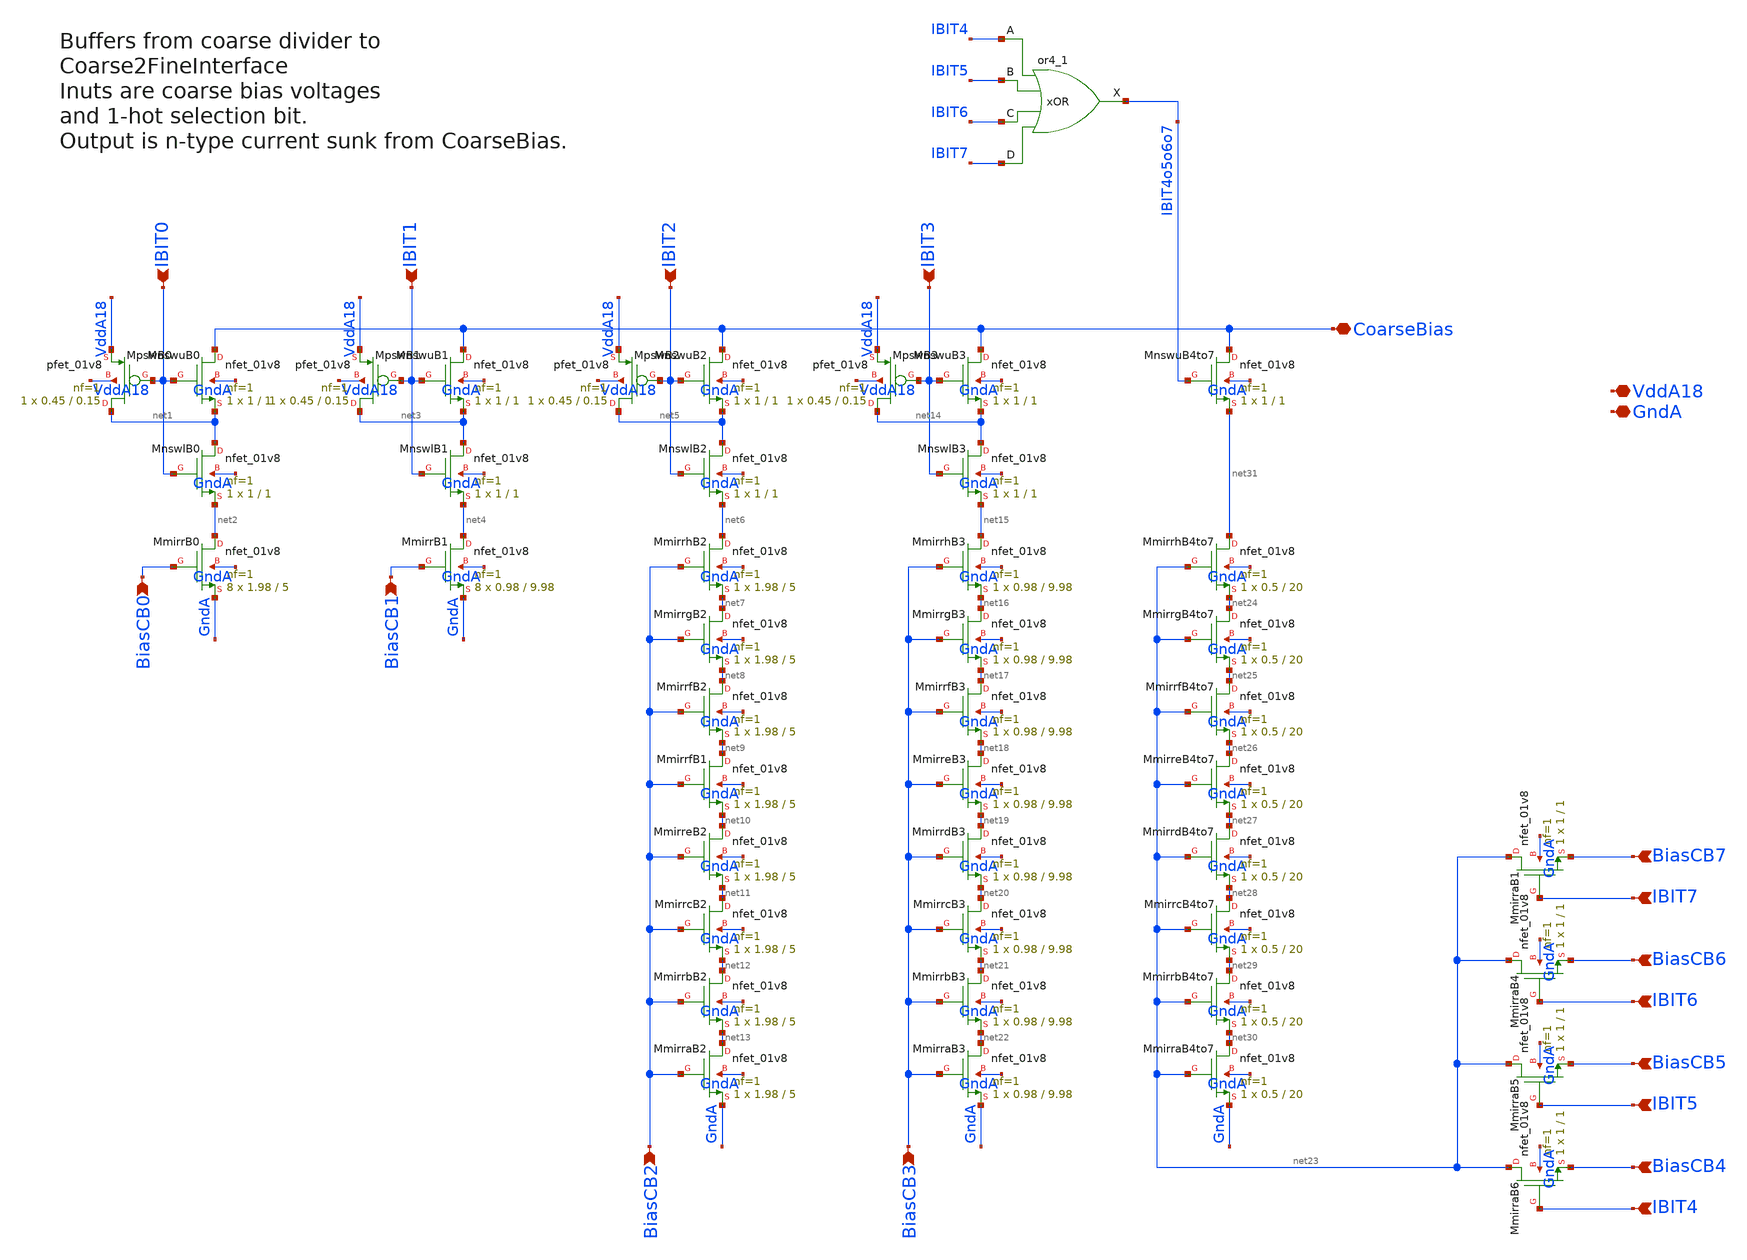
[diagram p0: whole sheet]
** sch_path: analog/xschem/BiasCoarseSel8to1.sch
**.subckt BiasCoarseSel8to1 IBIT0 BiasCB0 IBIT1 BiasCB1 IBIT2 BiasCB2 IBIT3 BiasCB3 BiasCB7 IBIT7
*+ BiasCB6 IBIT6 BiasCB5 IBIT5 BiasCB4 IBIT4 CoarseBias VddA18 GndA
*.ipin IBIT0
*.ipin BiasCB0
*.ipin IBIT1
*.ipin BiasCB1
*.ipin IBIT2
*.ipin BiasCB2
*.ipin IBIT3
*.ipin BiasCB3
*.ipin BiasCB7
*.ipin IBIT7
*.ipin BiasCB6
*.ipin IBIT6
*.ipin BiasCB5
*.ipin IBIT5
*.ipin BiasCB4
*.ipin IBIT4
*.iopin CoarseBias
*.iopin VddA18
*.iopin GndA
xOR IBIT4 IBIT5 IBIT6 IBIT7 GndA GndA VddA18 VddA18 IBIT4o5o6o7 sky130_fd_sc_hd__or4_1
XMpswB0 net1 IBIT0 VddA18 VddA18 sky130_fd_pr__pfet_01v8 L=0.15 W=0.45 nf=1 ad='int((1 + 1)/2) * 0.45 / 1 * 0.29'
+ as='int((1 + 2)/2) * 0.45 / 1 * 0.29' pd='2*int((1 + 1)/2) * (0.45 / 1 + 0.29)' ps='2*int((1 + 2)/2) * (0.45 / 1 + 0.29)'
+ nrd='0.29 / 0.45 ' nrs='0.29 / 0.45 ' sa=0 sb=0 sd=0 mult=1 m=1
XMnswuB0 CoarseBias IBIT0 net1 GndA sky130_fd_pr__nfet_01v8 L=1 W=1 nf=1 ad='int((1 + 1)/2) * 1 / 1 * 0.29'
+ as='int((1 + 2)/2) * 1 / 1 * 0.29' pd='2*int((1 + 1)/2) * (1 / 1 + 0.29)' ps='2*int((1 + 2)/2) * (1 / 1 + 0.29)'
+ nrd='0.29 / 1 ' nrs='0.29 / 1 ' sa=0 sb=0 sd=0 mult=1 m=1
XMnswlB0 net1 IBIT0 net2 GndA sky130_fd_pr__nfet_01v8 L=1 W=1 nf=1 ad='int((1 + 1)/2) * 1 / 1 * 0.29'
+ as='int((1 + 2)/2) * 1 / 1 * 0.29' pd='2*int((1 + 1)/2) * (1 / 1 + 0.29)' ps='2*int((1 + 2)/2) * (1 / 1 + 0.29)'
+ nrd='0.29 / 1 ' nrs='0.29 / 1 ' sa=0 sb=0 sd=0 mult=1 m=1
XMmirrB0 net2 BiasCB0 GndA GndA sky130_fd_pr__nfet_01v8 L=5 W=1.98 nf=1 ad='int((1 + 1)/2) * 1.98 / 1 * 0.29'
+ as='int((1 + 2)/2) * 1.98 / 1 * 0.29' pd='2*int((1 + 1)/2) * (1.98 / 1 + 0.29)' ps='2*int((1 + 2)/2) * (1.98 / 1 + 0.29)'
+ nrd='0.29 / 1.98 ' nrs='0.29 / 1.98 ' sa=0 sb=0 sd=0 mult=8 m=8
XMpswB1 net3 IBIT1 VddA18 VddA18 sky130_fd_pr__pfet_01v8 L=0.15 W=0.45 nf=1 ad='int((1 + 1)/2) * 0.45 / 1 * 0.29'
+ as='int((1 + 2)/2) * 0.45 / 1 * 0.29' pd='2*int((1 + 1)/2) * (0.45 / 1 + 0.29)' ps='2*int((1 + 2)/2) * (0.45 / 1 + 0.29)'
+ nrd='0.29 / 0.45 ' nrs='0.29 / 0.45 ' sa=0 sb=0 sd=0 mult=1 m=1
XMnswuB1 CoarseBias IBIT1 net3 GndA sky130_fd_pr__nfet_01v8 L=1 W=1 nf=1 ad='int((1 + 1)/2) * 1 / 1 * 0.29'
+ as='int((1 + 2)/2) * 1 / 1 * 0.29' pd='2*int((1 + 1)/2) * (1 / 1 + 0.29)' ps='2*int((1 + 2)/2) * (1 / 1 + 0.29)'
+ nrd='0.29 / 1 ' nrs='0.29 / 1 ' sa=0 sb=0 sd=0 mult=1 m=1
XMnswlB1 net3 IBIT1 net4 GndA sky130_fd_pr__nfet_01v8 L=1 W=1 nf=1 ad='int((1 + 1)/2) * 1 / 1 * 0.29'
+ as='int((1 + 2)/2) * 1 / 1 * 0.29' pd='2*int((1 + 1)/2) * (1 / 1 + 0.29)' ps='2*int((1 + 2)/2) * (1 / 1 + 0.29)'
+ nrd='0.29 / 1 ' nrs='0.29 / 1 ' sa=0 sb=0 sd=0 mult=1 m=1
XMmirrB1 net4 BiasCB1 GndA GndA sky130_fd_pr__nfet_01v8 L=9.98 W=0.98 nf=1 ad='int((1 + 1)/2) * 0.98 / 1 * 0.29'
+ as='int((1 + 2)/2) * 0.98 / 1 * 0.29' pd='2*int((1 + 1)/2) * (0.98 / 1 + 0.29)' ps='2*int((1 + 2)/2) * (0.98 / 1 + 0.29)'
+ nrd='0.29 / 0.98 ' nrs='0.29 / 0.98 ' sa=0 sb=0 sd=0 mult=8 m=8
XMpswB2 net5 IBIT2 VddA18 VddA18 sky130_fd_pr__pfet_01v8 L=0.15 W=0.45 nf=1 ad='int((1 + 1)/2) * 0.45 / 1 * 0.29'
+ as='int((1 + 2)/2) * 0.45 / 1 * 0.29' pd='2*int((1 + 1)/2) * (0.45 / 1 + 0.29)' ps='2*int((1 + 2)/2) * (0.45 / 1 + 0.29)'
+ nrd='0.29 / 0.45 ' nrs='0.29 / 0.45 ' sa=0 sb=0 sd=0 mult=1 m=1
XMnswuB2 CoarseBias IBIT2 net5 GndA sky130_fd_pr__nfet_01v8 L=1 W=1 nf=1 ad='int((1 + 1)/2) * 1 / 1 * 0.29'
+ as='int((1 + 2)/2) * 1 / 1 * 0.29' pd='2*int((1 + 1)/2) * (1 / 1 + 0.29)' ps='2*int((1 + 2)/2) * (1 / 1 + 0.29)'
+ nrd='0.29 / 1 ' nrs='0.29 / 1 ' sa=0 sb=0 sd=0 mult=1 m=1
XMnswlB2 net5 IBIT2 net6 GndA sky130_fd_pr__nfet_01v8 L=1 W=1 nf=1 ad='int((1 + 1)/2) * 1 / 1 * 0.29'
+ as='int((1 + 2)/2) * 1 / 1 * 0.29' pd='2*int((1 + 1)/2) * (1 / 1 + 0.29)' ps='2*int((1 + 2)/2) * (1 / 1 + 0.29)'
+ nrd='0.29 / 1 ' nrs='0.29 / 1 ' sa=0 sb=0 sd=0 mult=1 m=1
XMmirrhB2 net6 BiasCB2 net7 GndA sky130_fd_pr__nfet_01v8 L=5 W=1.98 nf=1 ad='int((1 + 1)/2) * 1.98 / 1 * 0.29'
+ as='int((1 + 2)/2) * 1.98 / 1 * 0.29' pd='2*int((1 + 1)/2) * (1.98 / 1 + 0.29)' ps='2*int((1 + 2)/2) * (1.98 / 1 + 0.29)'
+ nrd='0.29 / 1.98 ' nrs='0.29 / 1.98 ' sa=0 sb=0 sd=0 mult=1 m=1
XMmirrgB2 net7 BiasCB2 net8 GndA sky130_fd_pr__nfet_01v8 L=5 W=1.98 nf=1 ad='int((1 + 1)/2) * 1.98 / 1 * 0.29'
+ as='int((1 + 2)/2) * 1.98 / 1 * 0.29' pd='2*int((1 + 1)/2) * (1.98 / 1 + 0.29)' ps='2*int((1 + 2)/2) * (1.98 / 1 + 0.29)'
+ nrd='0.29 / 1.98 ' nrs='0.29 / 1.98 ' sa=0 sb=0 sd=0 mult=1 m=1
XMmirrfB2 net8 BiasCB2 net9 GndA sky130_fd_pr__nfet_01v8 L=5 W=1.98 nf=1 ad='int((1 + 1)/2) * 1.98 / 1 * 0.29'
+ as='int((1 + 2)/2) * 1.98 / 1 * 0.29' pd='2*int((1 + 1)/2) * (1.98 / 1 + 0.29)' ps='2*int((1 + 2)/2) * (1.98 / 1 + 0.29)'
+ nrd='0.29 / 1.98 ' nrs='0.29 / 1.98 ' sa=0 sb=0 sd=0 mult=1 m=1
XMmirrfB1 net9 BiasCB2 net10 GndA sky130_fd_pr__nfet_01v8 L=5 W=1.98 nf=1 ad='int((1 + 1)/2) * 1.98 / 1 * 0.29'
+ as='int((1 + 2)/2) * 1.98 / 1 * 0.29' pd='2*int((1 + 1)/2) * (1.98 / 1 + 0.29)' ps='2*int((1 + 2)/2) * (1.98 / 1 + 0.29)'
+ nrd='0.29 / 1.98 ' nrs='0.29 / 1.98 ' sa=0 sb=0 sd=0 mult=1 m=1
XMmirreB2 net10 BiasCB2 net11 GndA sky130_fd_pr__nfet_01v8 L=5 W=1.98 nf=1 ad='int((1 + 1)/2) * 1.98 / 1 * 0.29'
+ as='int((1 + 2)/2) * 1.98 / 1 * 0.29' pd='2*int((1 + 1)/2) * (1.98 / 1 + 0.29)' ps='2*int((1 + 2)/2) * (1.98 / 1 + 0.29)'
+ nrd='0.29 / 1.98 ' nrs='0.29 / 1.98 ' sa=0 sb=0 sd=0 mult=1 m=1
XMmirrcB2 net11 BiasCB2 net12 GndA sky130_fd_pr__nfet_01v8 L=5 W=1.98 nf=1 ad='int((1 + 1)/2) * 1.98 / 1 * 0.29'
+ as='int((1 + 2)/2) * 1.98 / 1 * 0.29' pd='2*int((1 + 1)/2) * (1.98 / 1 + 0.29)' ps='2*int((1 + 2)/2) * (1.98 / 1 + 0.29)'
+ nrd='0.29 / 1.98 ' nrs='0.29 / 1.98 ' sa=0 sb=0 sd=0 mult=1 m=1
XMmirrbB2 net12 BiasCB2 net13 GndA sky130_fd_pr__nfet_01v8 L=5 W=1.98 nf=1 ad='int((1 + 1)/2) * 1.98 / 1 * 0.29'
+ as='int((1 + 2)/2) * 1.98 / 1 * 0.29' pd='2*int((1 + 1)/2) * (1.98 / 1 + 0.29)' ps='2*int((1 + 2)/2) * (1.98 / 1 + 0.29)'
+ nrd='0.29 / 1.98 ' nrs='0.29 / 1.98 ' sa=0 sb=0 sd=0 mult=1 m=1
XMmirraB2 net13 BiasCB2 GndA GndA sky130_fd_pr__nfet_01v8 L=5 W=1.98 nf=1 ad='int((1 + 1)/2) * 1.98 / 1 * 0.29'
+ as='int((1 + 2)/2) * 1.98 / 1 * 0.29' pd='2*int((1 + 1)/2) * (1.98 / 1 + 0.29)' ps='2*int((1 + 2)/2) * (1.98 / 1 + 0.29)'
+ nrd='0.29 / 1.98 ' nrs='0.29 / 1.98 ' sa=0 sb=0 sd=0 mult=1 m=1
XMpswB3 net14 IBIT3 VddA18 VddA18 sky130_fd_pr__pfet_01v8 L=0.15 W=0.45 nf=1 ad='int((1 + 1)/2) * 0.45 / 1 * 0.29'
+ as='int((1 + 2)/2) * 0.45 / 1 * 0.29' pd='2*int((1 + 1)/2) * (0.45 / 1 + 0.29)' ps='2*int((1 + 2)/2) * (0.45 / 1 + 0.29)'
+ nrd='0.29 / 0.45 ' nrs='0.29 / 0.45 ' sa=0 sb=0 sd=0 mult=1 m=1
XMnswuB3 CoarseBias IBIT3 net14 GndA sky130_fd_pr__nfet_01v8 L=1 W=1 nf=1 ad='int((1 + 1)/2) * 1 / 1 * 0.29'
+ as='int((1 + 2)/2) * 1 / 1 * 0.29' pd='2*int((1 + 1)/2) * (1 / 1 + 0.29)' ps='2*int((1 + 2)/2) * (1 / 1 + 0.29)'
+ nrd='0.29 / 1 ' nrs='0.29 / 1 ' sa=0 sb=0 sd=0 mult=1 m=1
XMnswlB3 net14 IBIT3 net15 GndA sky130_fd_pr__nfet_01v8 L=1 W=1 nf=1 ad='int((1 + 1)/2) * 1 / 1 * 0.29'
+ as='int((1 + 2)/2) * 1 / 1 * 0.29' pd='2*int((1 + 1)/2) * (1 / 1 + 0.29)' ps='2*int((1 + 2)/2) * (1 / 1 + 0.29)'
+ nrd='0.29 / 1 ' nrs='0.29 / 1 ' sa=0 sb=0 sd=0 mult=1 m=1
XMmirrhB3 net15 BiasCB3 net16 GndA sky130_fd_pr__nfet_01v8 L=9.98 W=0.98 nf=1 ad='int((1 + 1)/2) * 0.98 / 1 * 0.29'
+ as='int((1 + 2)/2) * 0.98 / 1 * 0.29' pd='2*int((1 + 1)/2) * (0.98 / 1 + 0.29)' ps='2*int((1 + 2)/2) * (0.98 / 1 + 0.29)'
+ nrd='0.29 / 0.98 ' nrs='0.29 / 0.98 ' sa=0 sb=0 sd=0 mult=1 m=1
XMmirrgB3 net16 BiasCB3 net17 GndA sky130_fd_pr__nfet_01v8 L=9.98 W=0.98 nf=1 ad='int((1 + 1)/2) * 0.98 / 1 * 0.29'
+ as='int((1 + 2)/2) * 0.98 / 1 * 0.29' pd='2*int((1 + 1)/2) * (0.98 / 1 + 0.29)' ps='2*int((1 + 2)/2) * (0.98 / 1 + 0.29)'
+ nrd='0.29 / 0.98 ' nrs='0.29 / 0.98 ' sa=0 sb=0 sd=0 mult=1 m=1
XMmirrfB3 net17 BiasCB3 net18 GndA sky130_fd_pr__nfet_01v8 L=9.98 W=0.98 nf=1 ad='int((1 + 1)/2) * 0.98 / 1 * 0.29'
+ as='int((1 + 2)/2) * 0.98 / 1 * 0.29' pd='2*int((1 + 1)/2) * (0.98 / 1 + 0.29)' ps='2*int((1 + 2)/2) * (0.98 / 1 + 0.29)'
+ nrd='0.29 / 0.98 ' nrs='0.29 / 0.98 ' sa=0 sb=0 sd=0 mult=1 m=1
XMmirreB3 net18 BiasCB3 net19 GndA sky130_fd_pr__nfet_01v8 L=9.98 W=0.98 nf=1 ad='int((1 + 1)/2) * 0.98 / 1 * 0.29'
+ as='int((1 + 2)/2) * 0.98 / 1 * 0.29' pd='2*int((1 + 1)/2) * (0.98 / 1 + 0.29)' ps='2*int((1 + 2)/2) * (0.98 / 1 + 0.29)'
+ nrd='0.29 / 0.98 ' nrs='0.29 / 0.98 ' sa=0 sb=0 sd=0 mult=1 m=1
XMmirrdB3 net19 BiasCB3 net20 GndA sky130_fd_pr__nfet_01v8 L=9.98 W=0.98 nf=1 ad='int((1 + 1)/2) * 0.98 / 1 * 0.29'
+ as='int((1 + 2)/2) * 0.98 / 1 * 0.29' pd='2*int((1 + 1)/2) * (0.98 / 1 + 0.29)' ps='2*int((1 + 2)/2) * (0.98 / 1 + 0.29)'
+ nrd='0.29 / 0.98 ' nrs='0.29 / 0.98 ' sa=0 sb=0 sd=0 mult=1 m=1
XMmirrcB3 net20 BiasCB3 net21 GndA sky130_fd_pr__nfet_01v8 L=9.98 W=0.98 nf=1 ad='int((1 + 1)/2) * 0.98 / 1 * 0.29'
+ as='int((1 + 2)/2) * 0.98 / 1 * 0.29' pd='2*int((1 + 1)/2) * (0.98 / 1 + 0.29)' ps='2*int((1 + 2)/2) * (0.98 / 1 + 0.29)'
+ nrd='0.29 / 0.98 ' nrs='0.29 / 0.98 ' sa=0 sb=0 sd=0 mult=1 m=1
XMmirrbB3 net21 BiasCB3 net22 GndA sky130_fd_pr__nfet_01v8 L=9.98 W=0.98 nf=1 ad='int((1 + 1)/2) * 0.98 / 1 * 0.29'
+ as='int((1 + 2)/2) * 0.98 / 1 * 0.29' pd='2*int((1 + 1)/2) * (0.98 / 1 + 0.29)' ps='2*int((1 + 2)/2) * (0.98 / 1 + 0.29)'
+ nrd='0.29 / 0.98 ' nrs='0.29 / 0.98 ' sa=0 sb=0 sd=0 mult=1 m=1
XMmirraB3 net22 BiasCB3 GndA GndA sky130_fd_pr__nfet_01v8 L=9.98 W=0.98 nf=1 ad='int((1 + 1)/2) * 0.98 / 1 * 0.29'
+ as='int((1 + 2)/2) * 0.98 / 1 * 0.29' pd='2*int((1 + 1)/2) * (0.98 / 1 + 0.29)' ps='2*int((1 + 2)/2) * (0.98 / 1 + 0.29)'
+ nrd='0.29 / 0.98 ' nrs='0.29 / 0.98 ' sa=0 sb=0 sd=0 mult=1 m=1
XMnswuB4to7 CoarseBias IBIT4o5o6o7 net31 GndA sky130_fd_pr__nfet_01v8 L=1 W=1 nf=1 ad='int((1 + 1)/2) * 1 / 1 * 0.29'
+ as='int((1 + 2)/2) * 1 / 1 * 0.29' pd='2*int((1 + 1)/2) * (1 / 1 + 0.29)' ps='2*int((1 + 2)/2) * (1 / 1 + 0.29)'
+ nrd='0.29 / 1 ' nrs='0.29 / 1 ' sa=0 sb=0 sd=0 mult=1 m=1
XMmirrhB4to7 net31 net23 net24 GndA sky130_fd_pr__nfet_01v8 L=20 W=0.5 nf=1 ad='int((1 + 1)/2) * 0.5 / 1 * 0.29'
+ as='int((1 + 2)/2) * 0.5 / 1 * 0.29' pd='2*int((1 + 1)/2) * (0.5 / 1 + 0.29)' ps='2*int((1 + 2)/2) * (0.5 / 1 + 0.29)'
+ nrd='0.29 / 0.5 ' nrs='0.29 / 0.5 ' sa=0 sb=0 sd=0 mult=1 m=1
XMmirraB4to7 net30 net23 GndA GndA sky130_fd_pr__nfet_01v8 L=20 W=0.5 nf=1 ad='int((1 + 1)/2) * 0.5 / 1 * 0.29'
+ as='int((1 + 2)/2) * 0.5 / 1 * 0.29' pd='2*int((1 + 1)/2) * (0.5 / 1 + 0.29)' ps='2*int((1 + 2)/2) * (0.5 / 1 + 0.29)'
+ nrd='0.29 / 0.5 ' nrs='0.29 / 0.5 ' sa=0 sb=0 sd=0 mult=1 m=1
XMmirrbB4to7 net29 net23 net30 GndA sky130_fd_pr__nfet_01v8 L=20 W=0.5 nf=1 ad='int((1 + 1)/2) * 0.5 / 1 * 0.29'
+ as='int((1 + 2)/2) * 0.5 / 1 * 0.29' pd='2*int((1 + 1)/2) * (0.5 / 1 + 0.29)' ps='2*int((1 + 2)/2) * (0.5 / 1 + 0.29)'
+ nrd='0.29 / 0.5 ' nrs='0.29 / 0.5 ' sa=0 sb=0 sd=0 mult=1 m=1
XMmirrcB4to7 net28 net23 net29 GndA sky130_fd_pr__nfet_01v8 L=20 W=0.5 nf=1 ad='int((1 + 1)/2) * 0.5 / 1 * 0.29'
+ as='int((1 + 2)/2) * 0.5 / 1 * 0.29' pd='2*int((1 + 1)/2) * (0.5 / 1 + 0.29)' ps='2*int((1 + 2)/2) * (0.5 / 1 + 0.29)'
+ nrd='0.29 / 0.5 ' nrs='0.29 / 0.5 ' sa=0 sb=0 sd=0 mult=1 m=1
XMmirrdB4to7 net27 net23 net28 GndA sky130_fd_pr__nfet_01v8 L=20 W=0.5 nf=1 ad='int((1 + 1)/2) * 0.5 / 1 * 0.29'
+ as='int((1 + 2)/2) * 0.5 / 1 * 0.29' pd='2*int((1 + 1)/2) * (0.5 / 1 + 0.29)' ps='2*int((1 + 2)/2) * (0.5 / 1 + 0.29)'
+ nrd='0.29 / 0.5 ' nrs='0.29 / 0.5 ' sa=0 sb=0 sd=0 mult=1 m=1
XMmirreB4to7 net26 net23 net27 GndA sky130_fd_pr__nfet_01v8 L=20 W=0.5 nf=1 ad='int((1 + 1)/2) * 0.5 / 1 * 0.29'
+ as='int((1 + 2)/2) * 0.5 / 1 * 0.29' pd='2*int((1 + 1)/2) * (0.5 / 1 + 0.29)' ps='2*int((1 + 2)/2) * (0.5 / 1 + 0.29)'
+ nrd='0.29 / 0.5 ' nrs='0.29 / 0.5 ' sa=0 sb=0 sd=0 mult=1 m=1
XMmirrfB4to7 net25 net23 net26 GndA sky130_fd_pr__nfet_01v8 L=20 W=0.5 nf=1 ad='int((1 + 1)/2) * 0.5 / 1 * 0.29'
+ as='int((1 + 2)/2) * 0.5 / 1 * 0.29' pd='2*int((1 + 1)/2) * (0.5 / 1 + 0.29)' ps='2*int((1 + 2)/2) * (0.5 / 1 + 0.29)'
+ nrd='0.29 / 0.5 ' nrs='0.29 / 0.5 ' sa=0 sb=0 sd=0 mult=1 m=1
XMmirrgB4to7 net24 net23 net25 GndA sky130_fd_pr__nfet_01v8 L=20 W=0.5 nf=1 ad='int((1 + 1)/2) * 0.5 / 1 * 0.29'
+ as='int((1 + 2)/2) * 0.5 / 1 * 0.29' pd='2*int((1 + 1)/2) * (0.5 / 1 + 0.29)' ps='2*int((1 + 2)/2) * (0.5 / 1 + 0.29)'
+ nrd='0.29 / 0.5 ' nrs='0.29 / 0.5 ' sa=0 sb=0 sd=0 mult=1 m=1
XMmirraB1 net23 IBIT7 BiasCB7 GndA sky130_fd_pr__nfet_01v8 L=1 W=1 nf=1 ad='int((1 + 1)/2) * 1 / 1 * 0.29'
+ as='int((1 + 2)/2) * 1 / 1 * 0.29' pd='2*int((1 + 1)/2) * (1 / 1 + 0.29)' ps='2*int((1 + 2)/2) * (1 / 1 + 0.29)'
+ nrd='0.29 / 1 ' nrs='0.29 / 1 ' sa=0 sb=0 sd=0 mult=1 m=1
XMmirraB4 net23 IBIT6 BiasCB6 GndA sky130_fd_pr__nfet_01v8 L=1 W=1 nf=1 ad='int((1 + 1)/2) * 1 / 1 * 0.29'
+ as='int((1 + 2)/2) * 1 / 1 * 0.29' pd='2*int((1 + 1)/2) * (1 / 1 + 0.29)' ps='2*int((1 + 2)/2) * (1 / 1 + 0.29)'
+ nrd='0.29 / 1 ' nrs='0.29 / 1 ' sa=0 sb=0 sd=0 mult=1 m=1
XMmirraB5 net23 IBIT5 BiasCB5 GndA sky130_fd_pr__nfet_01v8 L=1 W=1 nf=1 ad='int((1 + 1)/2) * 1 / 1 * 0.29'
+ as='int((1 + 2)/2) * 1 / 1 * 0.29' pd='2*int((1 + 1)/2) * (1 / 1 + 0.29)' ps='2*int((1 + 2)/2) * (1 / 1 + 0.29)'
+ nrd='0.29 / 1 ' nrs='0.29 / 1 ' sa=0 sb=0 sd=0 mult=1 m=1
XMmirraB6 net23 IBIT4 BiasCB4 GndA sky130_fd_pr__nfet_01v8 L=1 W=1 nf=1 ad='int((1 + 1)/2) * 1 / 1 * 0.29'
+ as='int((1 + 2)/2) * 1 / 1 * 0.29' pd='2*int((1 + 1)/2) * (1 / 1 + 0.29)' ps='2*int((1 + 2)/2) * (1 / 1 + 0.29)'
+ nrd='0.29 / 1 ' nrs='0.29 / 1 ' sa=0 sb=0 sd=0 mult=1 m=1
**.ends
.end
